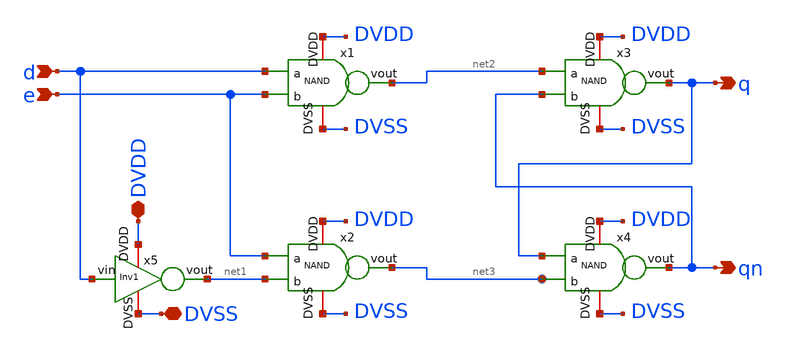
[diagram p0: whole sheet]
** sch_path: src/schematic/DFF/DLATCH.sch
**.subckt DLATCH d e DVDD DVSS q qn
*.ipin d
*.ipin e
*.iopin DVDD
*.iopin DVSS
*.opin q
*.opin qn
x1 DVDD net2 d e DVSS NAND
x2 DVDD net3 e net1 DVSS NAND
x3 DVDD q net2 qn DVSS NAND
x4 DVDD qn q net3 DVSS NAND
x5 DVDD d net1 DVSS Inv1
**.ends

* expanding   symbol:  Chipaton2026/src/schematic/DFF/NAND.sym # of pins=5
** sym_path: src/schematic/NAND/NAND.sym
** sch_path: src/schematic/NAND/NAND.sch
.subckt NAND DVDD vout a b DVSS
*.ipin a
*.opin vout
*.iopin DVDD
*.iopin DVSS
*.ipin b
XM3 vout a DVDD DVDD pfet_03v3 L=0.3u W=1.7u nf=1 ad='int((nf+1)/2) * W/nf * 0.18u' as='int((nf+2)/2) * W/nf * 0.18u'
+ pd='2*int((nf+1)/2) * (W/nf + 0.18u)' ps='2*int((nf+2)/2) * (W/nf + 0.18u)' nrd='0.18u / W' nrs='0.18u / W'
+ sa=0 sb=0 sd=0 m=1
XM4 vout a net1 DVSS nfet_03v3 L=0.3u W=0.85u nf=1 ad='int((nf+1)/2) * W/nf * 0.18u' as='int((nf+2)/2) * W/nf * 0.18u'
+ pd='2*int((nf+1)/2) * (W/nf + 0.18u)' ps='2*int((nf+2)/2) * (W/nf + 0.18u)' nrd='0.18u / W' nrs='0.18u / W'
+ sa=0 sb=0 sd=0 m=1
XM1 vout b DVDD DVDD pfet_03v3 L=0.3u W=1.7u nf=1 ad='int((nf+1)/2) * W/nf * 0.18u' as='int((nf+2)/2) * W/nf * 0.18u'
+ pd='2*int((nf+1)/2) * (W/nf + 0.18u)' ps='2*int((nf+2)/2) * (W/nf + 0.18u)' nrd='0.18u / W' nrs='0.18u / W'
+ sa=0 sb=0 sd=0 m=1
XM2 net1 b DVSS DVSS nfet_03v3 L=0.3u W=0.85u nf=1 ad='int((nf+1)/2) * W/nf * 0.18u' as='int((nf+2)/2) * W/nf * 0.18u'
+ pd='2*int((nf+1)/2) * (W/nf + 0.18u)' ps='2*int((nf+2)/2) * (W/nf + 0.18u)' nrd='0.18u / W' nrs='0.18u / W'
+ sa=0 sb=0 sd=0 m=1
.ends


* expanding   symbol:  Chipaton2026/src/schematic/DFF/Inv1.sym # of pins=4
** sym_path: src/schematic/INV/Inv1.sym
** sch_path: src/schematic/INV/Inv1.sch
.subckt Inv1 DVDD vin vout DVSS
*.ipin vin
*.opin vout
*.iopin DVDD
*.iopin DVSS
XM3 vout vin DVDD DVDD pfet_03v3 L=0.3u W=1.7u nf=1 ad='int((nf+1)/2) * W/nf * 0.18u' as='int((nf+2)/2) * W/nf * 0.18u'
+ pd='2*int((nf+1)/2) * (W/nf + 0.18u)' ps='2*int((nf+2)/2) * (W/nf + 0.18u)' nrd='0.18u / W' nrs='0.18u / W'
+ sa=0 sb=0 sd=0 m=1
XM4 vout vin DVSS DVSS nfet_03v3 L=0.3u W=0.85u nf=1 ad='int((nf+1)/2) * W/nf * 0.18u' as='int((nf+2)/2) * W/nf * 0.18u'
+ pd='2*int((nf+1)/2) * (W/nf + 0.18u)' ps='2*int((nf+2)/2) * (W/nf + 0.18u)' nrd='0.18u / W' nrs='0.18u / W'
+ sa=0 sb=0 sd=0 m=1
.ends

.end
